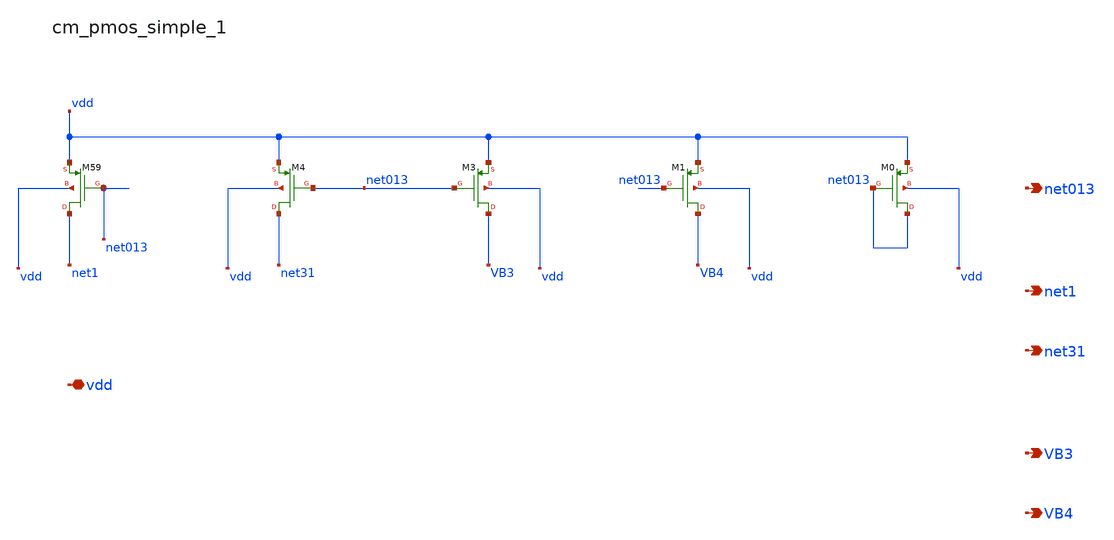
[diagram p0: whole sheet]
** sch_path: analog-db/raw/amp_016_song_dacfc/hier/blocks/cm_pmos_simple_1.sch
**.subckt cm_pmos_simple_1 vdd net013 net1 net31 VB3 VB4
*.iopin vdd
*.opin net013
*.opin net1
*.opin net31
*.opin VB3
*.opin VB4
XM0 net013 net013 vdd vdd sg13_lv_pmos w=x_dut_xm0_w l=x_dut_xm0_l ng=1 m=x_dut_xm0_m
XM1 VB4 net013 vdd vdd sg13_lv_pmos w=x_dut_xm1_w l=x_dut_xm1_l ng=1 m=x_dut_xm1_m
XM3 VB3 net013 vdd vdd sg13_lv_pmos w=x_dut_xm3_w l=x_dut_xm3_l ng=1 m=x_dut_xm3_m
XM4 net31 net013 vdd vdd sg13_lv_pmos w=x_dut_xm4_w l=x_dut_xm4_l ng=1 m=x_dut_xm4_m
XM59 net1 net013 vdd vdd sg13_lv_pmos w=x_dut_xm59_w l=x_dut_xm59_l ng=1 m=x_dut_xm59_m
**.ends
.end
